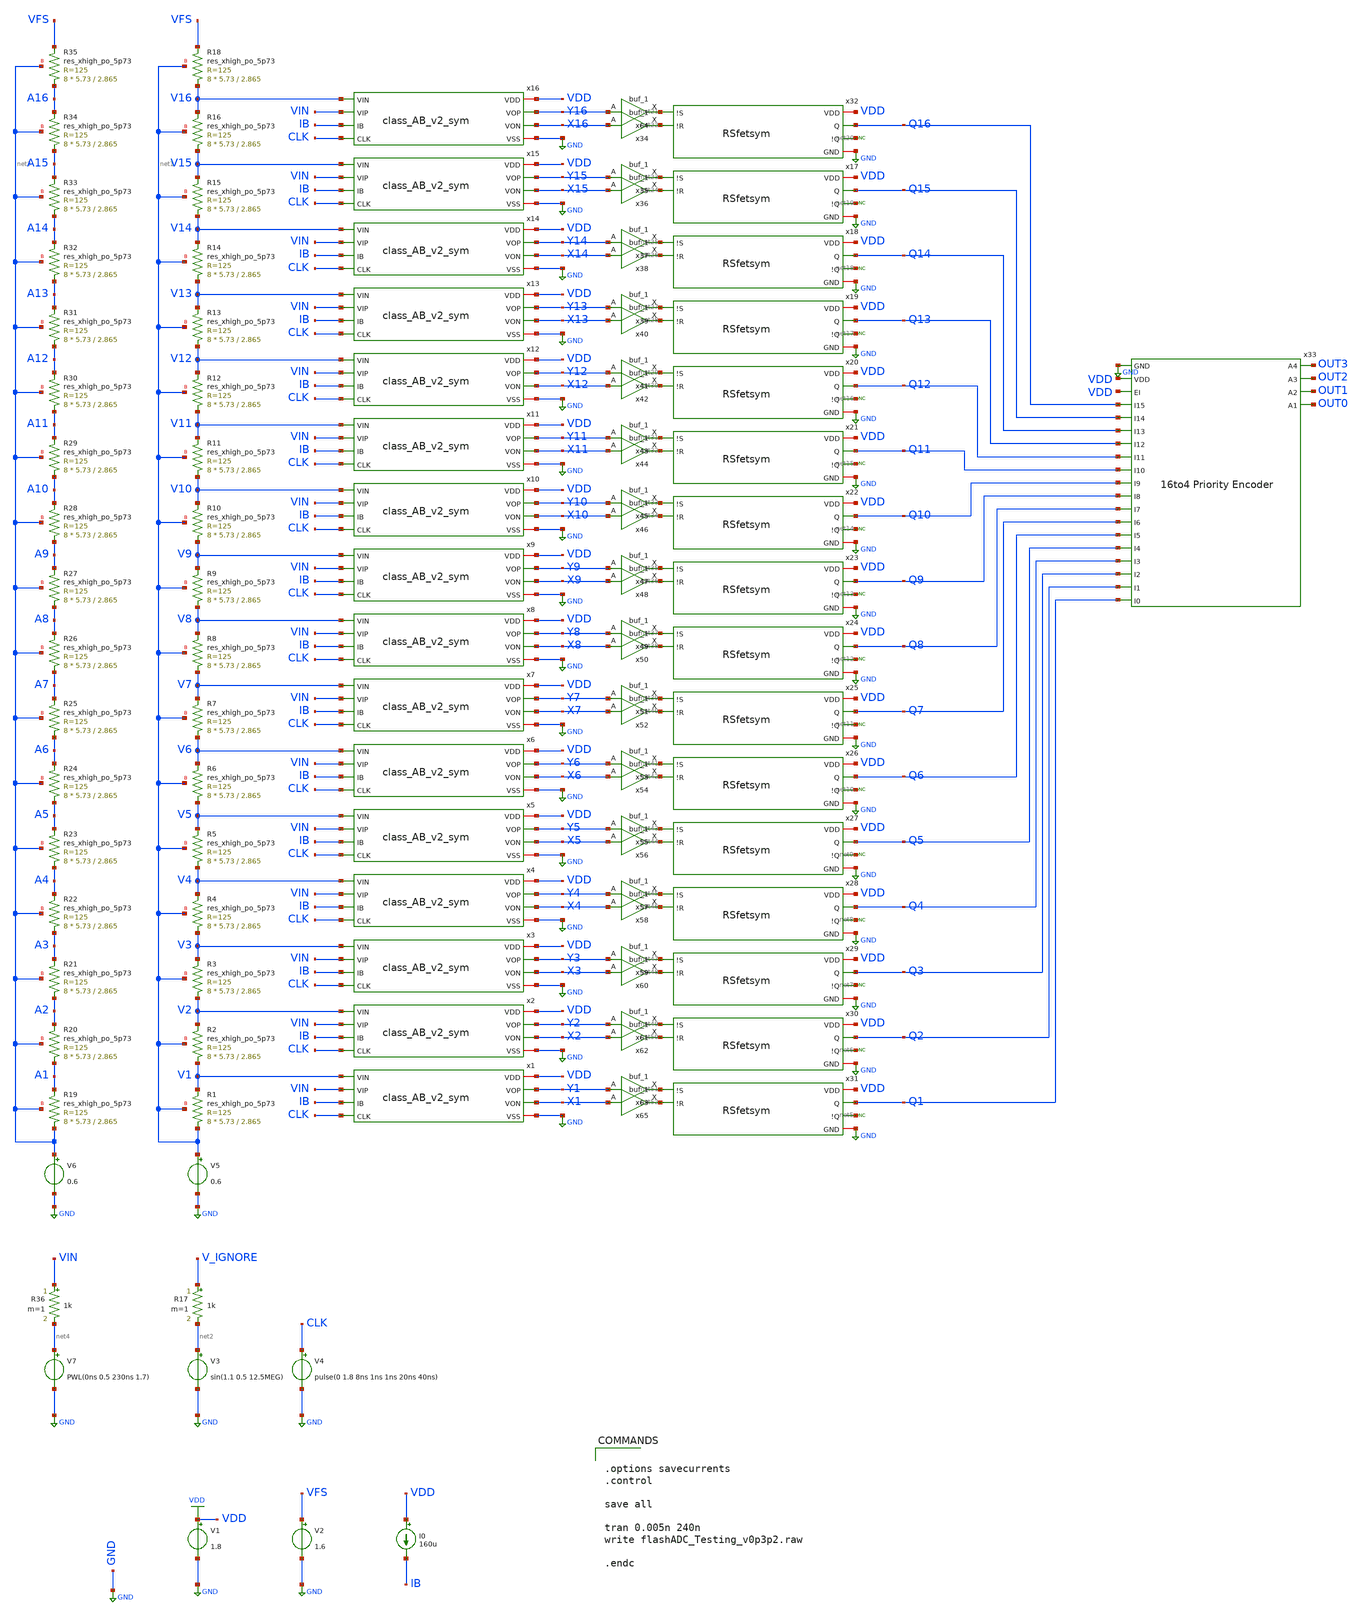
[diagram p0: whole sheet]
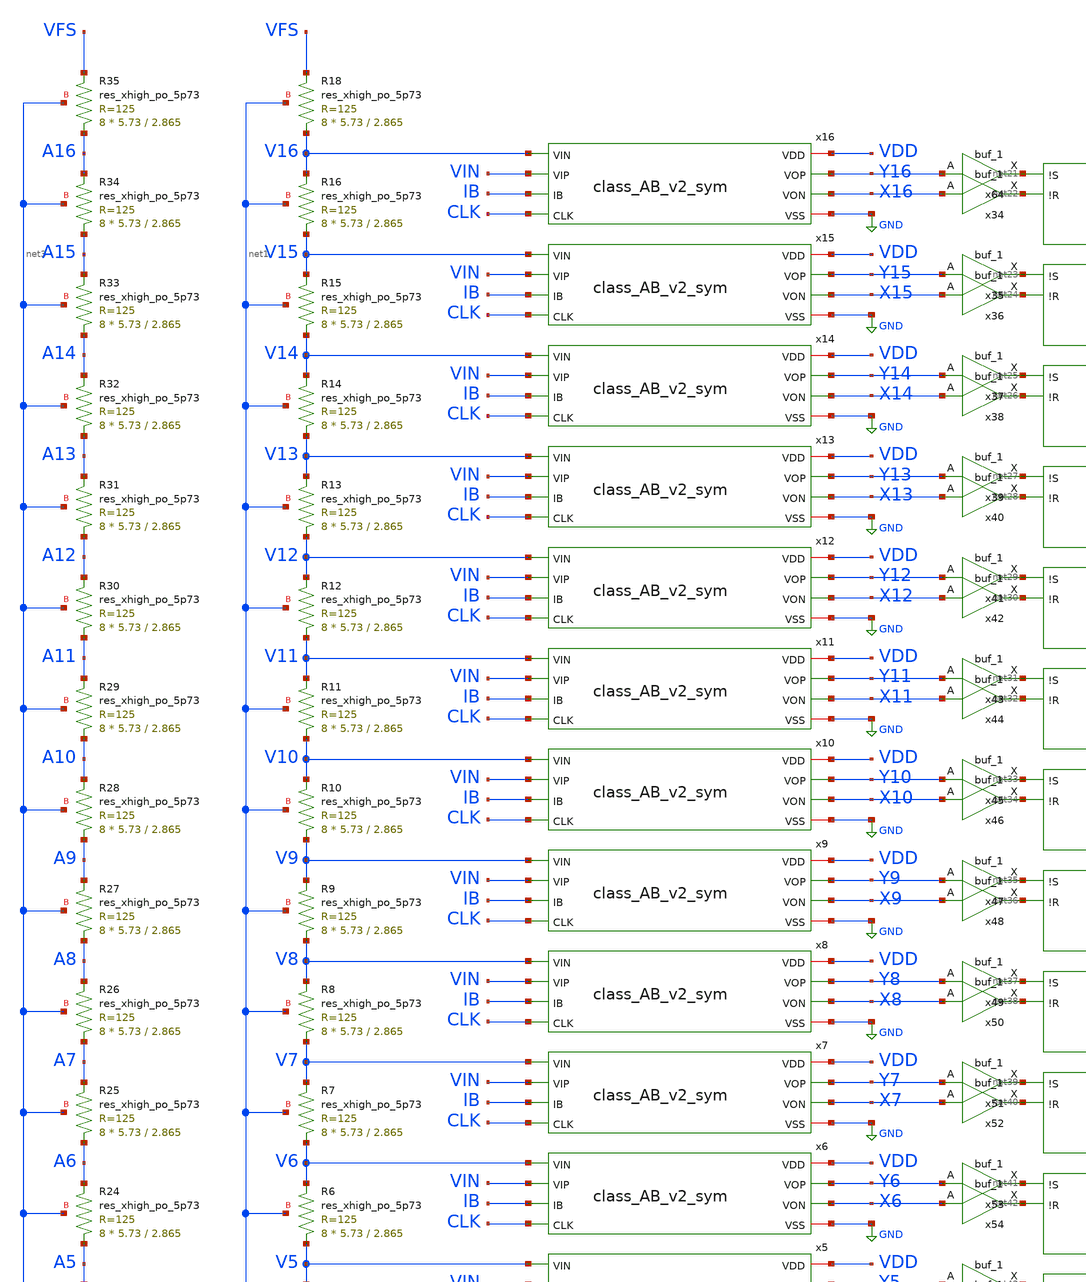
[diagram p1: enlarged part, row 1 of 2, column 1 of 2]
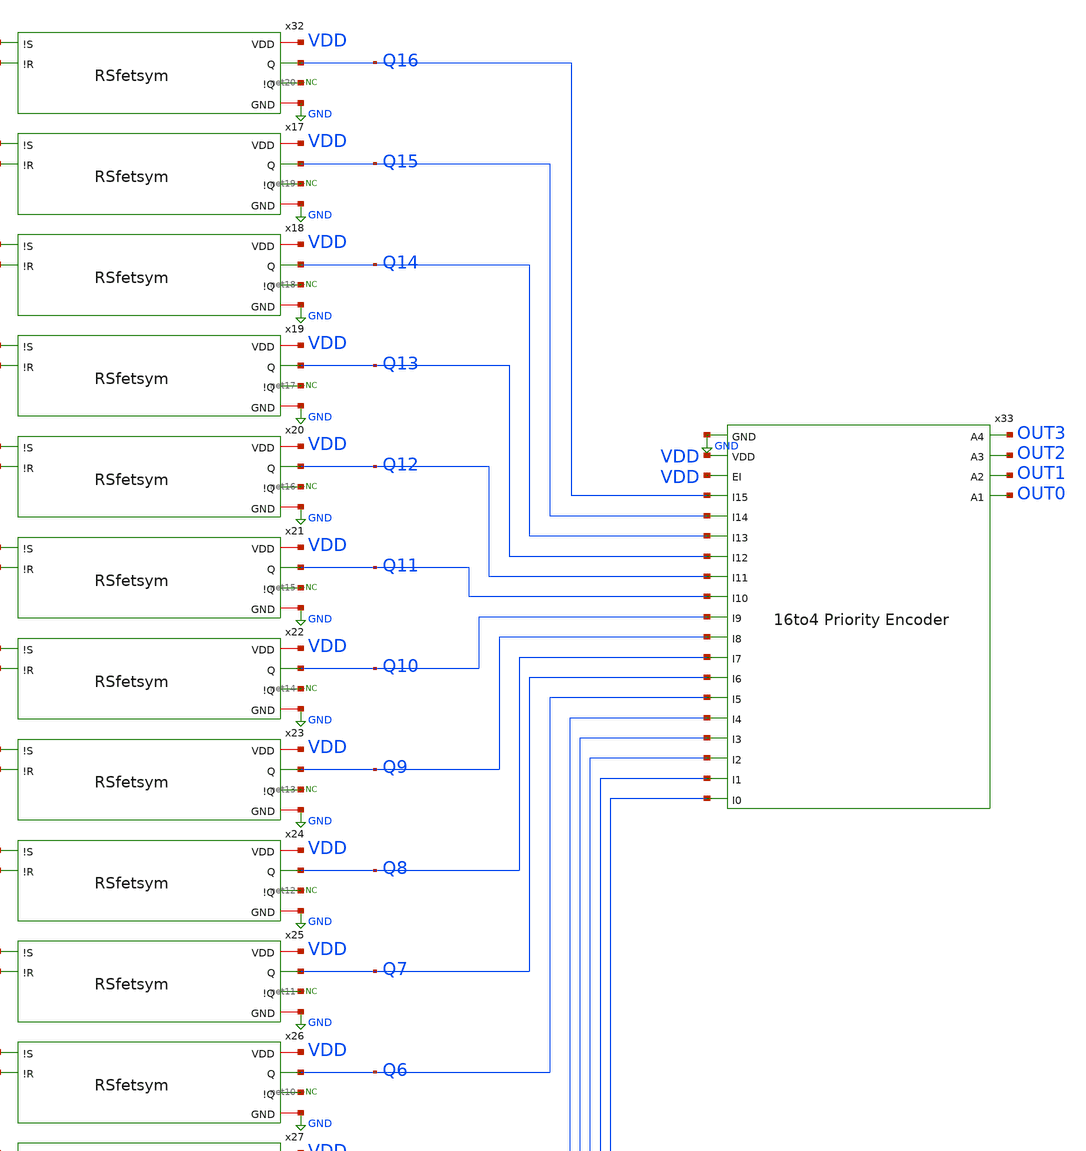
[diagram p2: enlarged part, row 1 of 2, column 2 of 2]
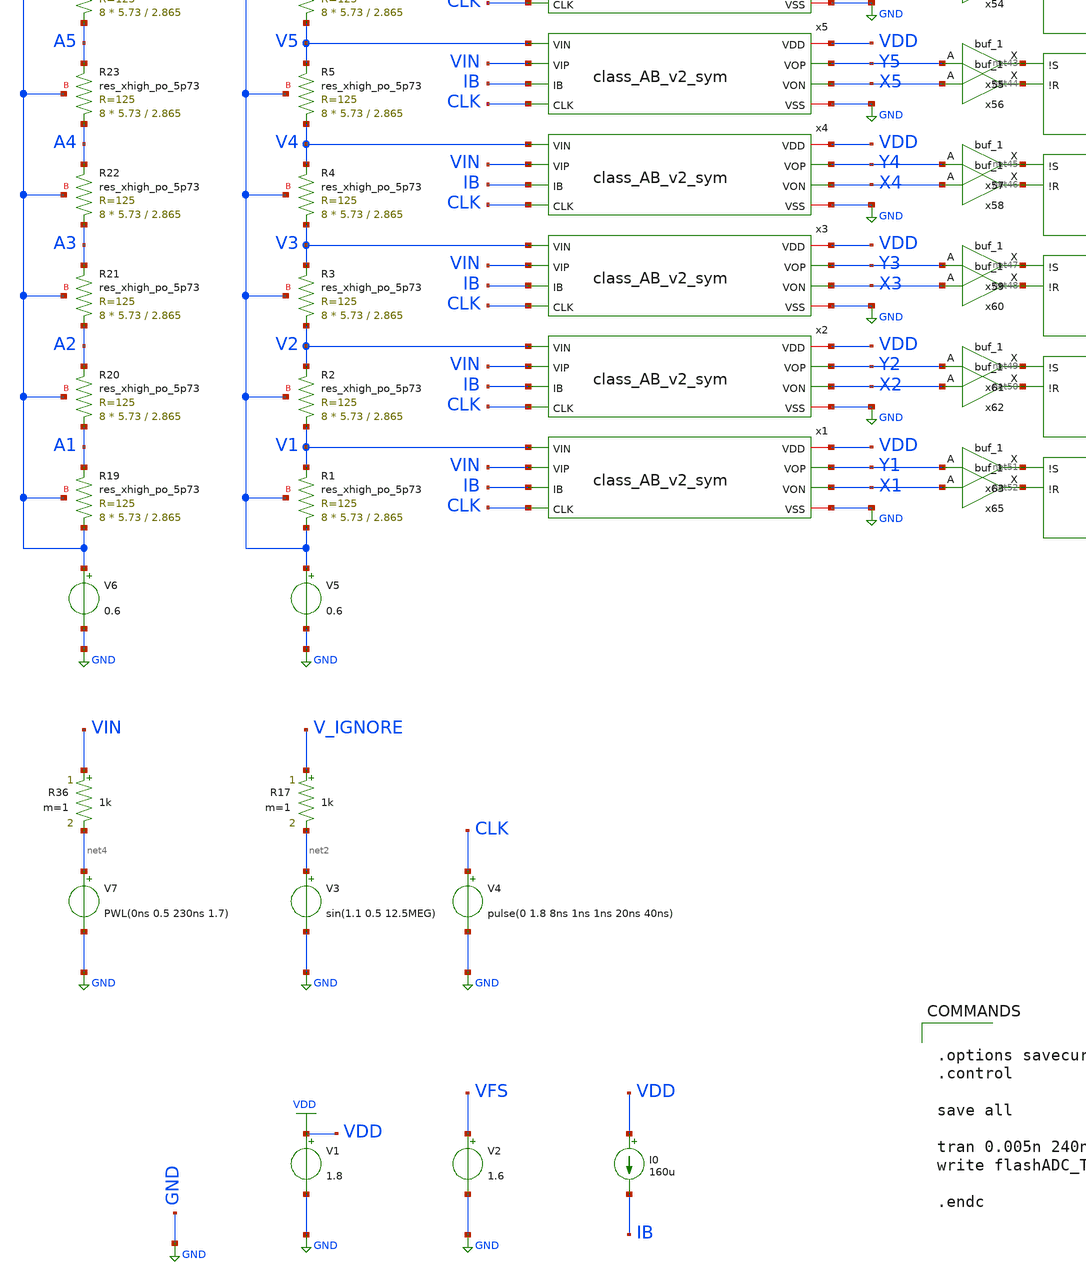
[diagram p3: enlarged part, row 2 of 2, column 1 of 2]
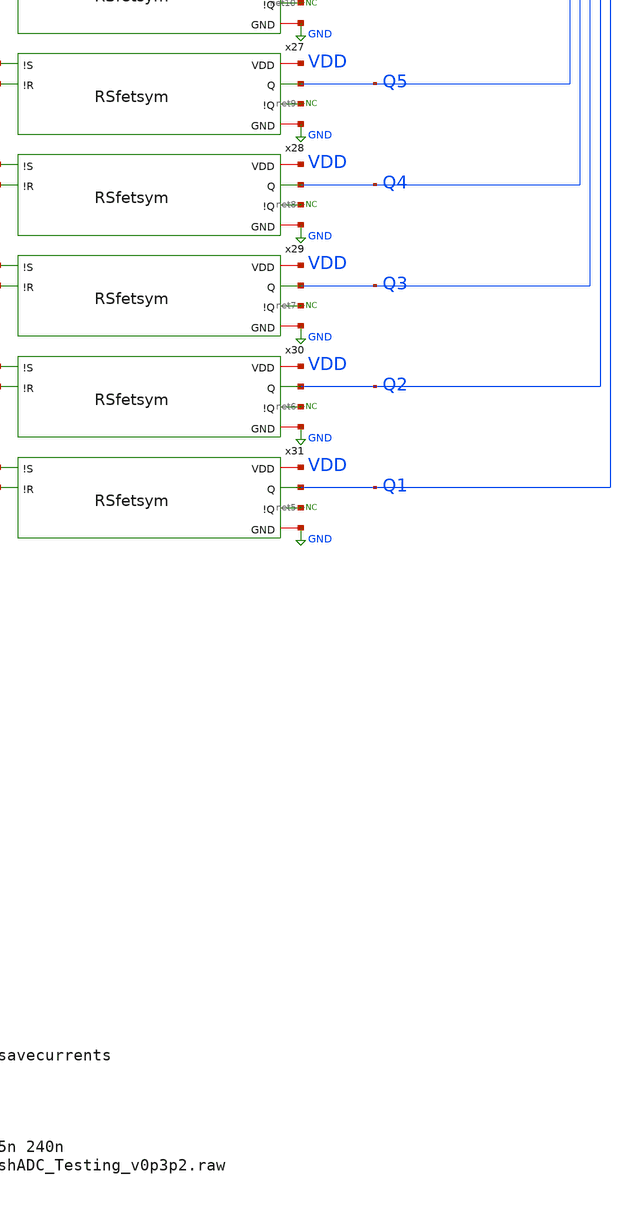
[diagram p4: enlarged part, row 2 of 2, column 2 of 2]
** sch_path: flashADC/xschem/flashADC_Symbolize_v0p4p2.sch
.lib $::SKYWATER_MODELS/sky130.lib.spice tt
.include $::SKYWATER_STDCELLS/sky130_fd_sc_hd.spice

**.subckt flashADC_Symbolize_v0p4p2
V3 net2 GND sin(1.1 0.5 12.5MEG)
V4 CLK GND pulse(0 1.8 8ns 1ns 1ns 20ns 40ns)
V1 VDD GND 1.8
V2 VFS GND 1.6
R17 V_IGNORE net2 1k m=1
I0 VDD IB 160u
V5 net1 GND 0.6
XR19 net3 A1 net3 sky130_fd_pr__res_xhigh_po_5p73 L=2.865 mult=8 m=8
V6 net3 GND 0.6
XR20 A1 A2 net3 sky130_fd_pr__res_xhigh_po_5p73 L=2.865 mult=8 m=8
XR21 A2 A3 net3 sky130_fd_pr__res_xhigh_po_5p73 L=2.865 mult=8 m=8
XR22 A3 A4 net3 sky130_fd_pr__res_xhigh_po_5p73 L=2.865 mult=8 m=8
XR23 A4 A5 net3 sky130_fd_pr__res_xhigh_po_5p73 L=2.865 mult=8 m=8
XR24 A5 A6 net3 sky130_fd_pr__res_xhigh_po_5p73 L=2.865 mult=8 m=8
XR25 A6 A7 net3 sky130_fd_pr__res_xhigh_po_5p73 L=2.865 mult=8 m=8
XR26 A7 A8 net3 sky130_fd_pr__res_xhigh_po_5p73 L=2.865 mult=8 m=8
XR27 A8 A9 net3 sky130_fd_pr__res_xhigh_po_5p73 L=2.865 mult=8 m=8
XR28 A9 A10 net3 sky130_fd_pr__res_xhigh_po_5p73 L=2.865 mult=8 m=8
XR29 A10 A11 net3 sky130_fd_pr__res_xhigh_po_5p73 L=2.865 mult=8 m=8
XR30 A11 A12 net3 sky130_fd_pr__res_xhigh_po_5p73 L=2.865 mult=8 m=8
XR31 A12 A13 net3 sky130_fd_pr__res_xhigh_po_5p73 L=2.865 mult=8 m=8
XR32 A13 A14 net3 sky130_fd_pr__res_xhigh_po_5p73 L=2.865 mult=8 m=8
XR33 A14 A15 net3 sky130_fd_pr__res_xhigh_po_5p73 L=2.865 mult=8 m=8
XR34 A15 A16 net3 sky130_fd_pr__res_xhigh_po_5p73 L=2.865 mult=8 m=8
XR35 A16 VFS net3 sky130_fd_pr__res_xhigh_po_5p73 L=2.865 mult=8 m=8
XR1 net1 V1 net1 sky130_fd_pr__res_xhigh_po_5p73 L=2.865 mult=8 m=8
XR2 V1 V2 net1 sky130_fd_pr__res_xhigh_po_5p73 L=2.865 mult=8 m=8
XR3 V2 V3 net1 sky130_fd_pr__res_xhigh_po_5p73 L=2.865 mult=8 m=8
XR4 V3 V4 net1 sky130_fd_pr__res_xhigh_po_5p73 L=2.865 mult=8 m=8
XR5 V4 V5 net1 sky130_fd_pr__res_xhigh_po_5p73 L=2.865 mult=8 m=8
XR6 V5 V6 net1 sky130_fd_pr__res_xhigh_po_5p73 L=2.865 mult=8 m=8
XR7 V6 V7 net1 sky130_fd_pr__res_xhigh_po_5p73 L=2.865 mult=8 m=8
XR8 V7 V8 net1 sky130_fd_pr__res_xhigh_po_5p73 L=2.865 mult=8 m=8
XR9 V8 V9 net1 sky130_fd_pr__res_xhigh_po_5p73 L=2.865 mult=8 m=8
XR10 V9 V10 net1 sky130_fd_pr__res_xhigh_po_5p73 L=2.865 mult=8 m=8
XR11 V10 V11 net1 sky130_fd_pr__res_xhigh_po_5p73 L=2.865 mult=8 m=8
XR12 V11 V12 net1 sky130_fd_pr__res_xhigh_po_5p73 L=2.865 mult=8 m=8
XR13 V12 V13 net1 sky130_fd_pr__res_xhigh_po_5p73 L=2.865 mult=8 m=8
XR14 V13 V14 net1 sky130_fd_pr__res_xhigh_po_5p73 L=2.865 mult=8 m=8
XR15 V14 V15 net1 sky130_fd_pr__res_xhigh_po_5p73 L=2.865 mult=8 m=8
XR16 V15 V16 net1 sky130_fd_pr__res_xhigh_po_5p73 L=2.865 mult=8 m=8
XR18 V16 VFS net1 sky130_fd_pr__res_xhigh_po_5p73 L=2.865 mult=8 m=8
V7 net4 GND PWL(0ns 0.5 230ns 1.7)
R36 VIN net4 1k m=1
x1 VDD Y1 X1 V1 VIN IB CLK GND class_AB_v2_sym
x2 VDD Y2 X2 V2 VIN IB CLK GND class_AB_v2_sym
x3 VDD Y3 X3 V3 VIN IB CLK GND class_AB_v2_sym
x4 VDD Y4 X4 V4 VIN IB CLK GND class_AB_v2_sym
x5 VDD Y5 X5 V5 VIN IB CLK GND class_AB_v2_sym
x6 VDD Y6 X6 V6 VIN IB CLK GND class_AB_v2_sym
x7 VDD Y7 X7 V7 VIN IB CLK GND class_AB_v2_sym
x8 VDD Y8 X8 V8 VIN IB CLK GND class_AB_v2_sym
x9 VDD Y9 X9 V9 VIN IB CLK GND class_AB_v2_sym
x10 VDD Y10 X10 V10 VIN IB CLK GND class_AB_v2_sym
x11 VDD Y11 X11 V11 VIN IB CLK GND class_AB_v2_sym
x12 VDD Y12 X12 V12 VIN IB CLK GND class_AB_v2_sym
x13 VDD Y13 X13 V13 VIN IB CLK GND class_AB_v2_sym
x14 VDD Y14 X14 V14 VIN IB CLK GND class_AB_v2_sym
x15 VDD Y15 X15 V15 VIN IB CLK GND class_AB_v2_sym
x16 VDD Y16 X16 V16 VIN IB CLK GND class_AB_v2_sym
* noconn #net5
* noconn #net6
* noconn #net7
* noconn #net8
* noconn #net9
* noconn #net10
* noconn #net11
* noconn #net12
* noconn #net13
* noconn #net14
* noconn #net15
* noconn #net16
* noconn #net17
* noconn #net18
* noconn #net19
* noconn #net20
x32 VDD net21 net22 Q16 net20 GND RSfetsym
x17 VDD net23 net24 Q15 net19 GND RSfetsym
x18 VDD net25 net26 Q14 net18 GND RSfetsym
x19 VDD net27 net28 Q13 net17 GND RSfetsym
x20 VDD net29 net30 Q12 net16 GND RSfetsym
x21 VDD net31 net32 Q11 net15 GND RSfetsym
x22 VDD net33 net34 Q10 net14 GND RSfetsym
x23 VDD net35 net36 Q9 net13 GND RSfetsym
x24 VDD net37 net38 Q8 net12 GND RSfetsym
x25 VDD net39 net40 Q7 net11 GND RSfetsym
x26 VDD net41 net42 Q6 net10 GND RSfetsym
x27 VDD net43 net44 Q5 net9 GND RSfetsym
x28 VDD net45 net46 Q4 net8 GND RSfetsym
x29 VDD net47 net48 Q3 net7 GND RSfetsym
x30 VDD net49 net50 Q2 net6 GND RSfetsym
x31 VDD net51 net52 Q1 net5 GND RSfetsym
x33 GND VDD OUT3 VDD Q16 Q15 Q14 Q13 Q12 Q11 OUT2 Q10 Q9 Q8 Q7 Q6 Q5 OUT1 Q4 Q3 Q2 Q1 OUT0
+ 16to4_PriorityEncoder_v0p0p1
x64 Y16 GND GND VDD VDD net21 sky130_fd_sc_hd__buf_1
x34 X16 GND GND VDD VDD net22 sky130_fd_sc_hd__buf_1
x35 Y15 GND GND VDD VDD net23 sky130_fd_sc_hd__buf_1
x36 X15 GND GND VDD VDD net24 sky130_fd_sc_hd__buf_1
x37 Y14 GND GND VDD VDD net25 sky130_fd_sc_hd__buf_1
x38 X14 GND GND VDD VDD net26 sky130_fd_sc_hd__buf_1
x39 Y13 GND GND VDD VDD net27 sky130_fd_sc_hd__buf_1
x40 X13 GND GND VDD VDD net28 sky130_fd_sc_hd__buf_1
x41 Y12 GND GND VDD VDD net29 sky130_fd_sc_hd__buf_1
x42 X12 GND GND VDD VDD net30 sky130_fd_sc_hd__buf_1
x43 Y11 GND GND VDD VDD net31 sky130_fd_sc_hd__buf_1
x44 X11 GND GND VDD VDD net32 sky130_fd_sc_hd__buf_1
x45 Y10 GND GND VDD VDD net33 sky130_fd_sc_hd__buf_1
x46 X10 GND GND VDD VDD net34 sky130_fd_sc_hd__buf_1
x47 Y9 GND GND VDD VDD net35 sky130_fd_sc_hd__buf_1
x48 X9 GND GND VDD VDD net36 sky130_fd_sc_hd__buf_1
x49 Y8 GND GND VDD VDD net37 sky130_fd_sc_hd__buf_1
x50 X8 GND GND VDD VDD net38 sky130_fd_sc_hd__buf_1
x51 Y7 GND GND VDD VDD net39 sky130_fd_sc_hd__buf_1
x52 X7 GND GND VDD VDD net40 sky130_fd_sc_hd__buf_1
x53 Y6 GND GND VDD VDD net41 sky130_fd_sc_hd__buf_1
x54 X6 GND GND VDD VDD net42 sky130_fd_sc_hd__buf_1
x55 Y5 GND GND VDD VDD net43 sky130_fd_sc_hd__buf_1
x56 X5 GND GND VDD VDD net44 sky130_fd_sc_hd__buf_1
x57 Y4 GND GND VDD VDD net45 sky130_fd_sc_hd__buf_1
x58 X4 GND GND VDD VDD net46 sky130_fd_sc_hd__buf_1
x59 Y3 GND GND VDD VDD net47 sky130_fd_sc_hd__buf_1
x60 X3 GND GND VDD VDD net48 sky130_fd_sc_hd__buf_1
x61 Y2 GND GND VDD VDD net49 sky130_fd_sc_hd__buf_1
x62 X2 GND GND VDD VDD net50 sky130_fd_sc_hd__buf_1
x63 Y1 GND GND VDD VDD net51 sky130_fd_sc_hd__buf_1
x65 X1 GND GND VDD VDD net52 sky130_fd_sc_hd__buf_1
**** begin user architecture code


.options savecurrents
.control

save all

tran 0.005n 240n
write flashADC_Testing_v0p3p2.raw

.endc


**** end user architecture code
**.ends
.GLOBAL GND
.GLOBAL VDD
.end
